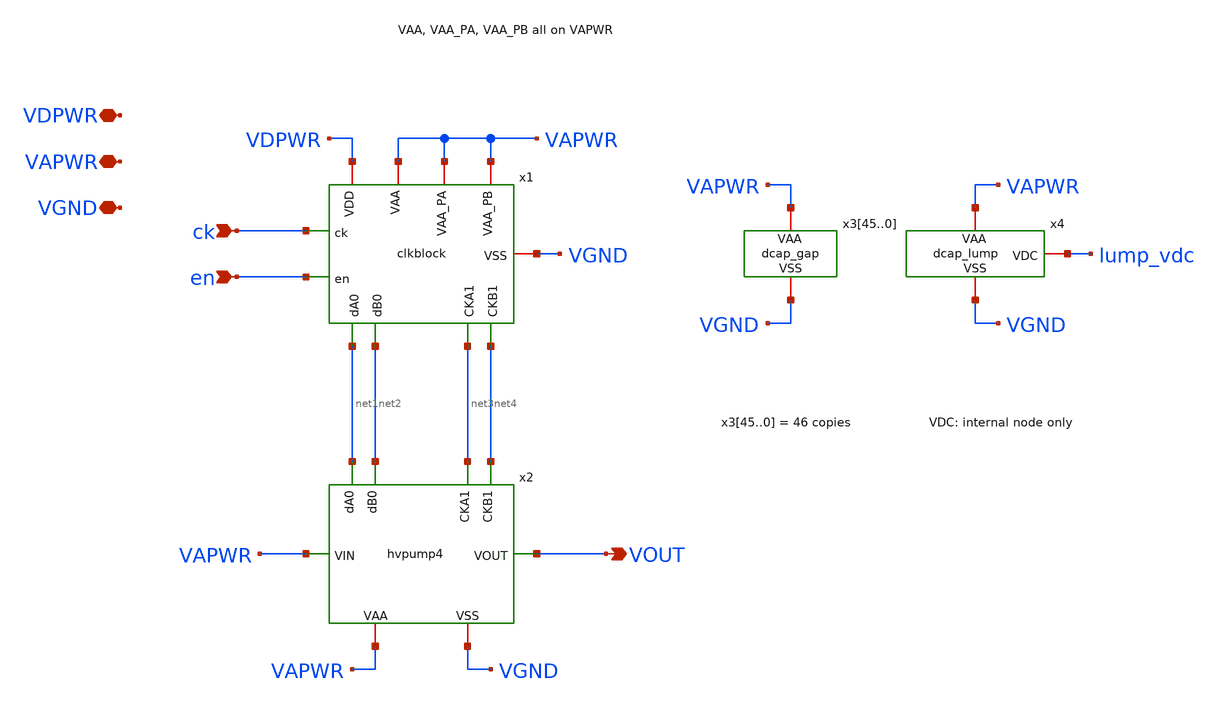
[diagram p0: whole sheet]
** sch_path: xschem/subsystem.sch
**.subckt subsystem VDPWR VAPWR VOUT en ck VGND
*.iopin VDPWR
*.iopin VAPWR
*.opin VOUT
*.ipin en
*.ipin ck
*.iopin VGND
x1 net3 net4 net1 net2 ck en VAPWR VDPWR VAPWR VAPWR VGND clkblock
x2 net1 net2 VAPWR VOUT net3 net4 VAPWR VGND hvpump4
x345 VGND VAPWR dcap_gap
x344 VGND VAPWR dcap_gap
x343 VGND VAPWR dcap_gap
x342 VGND VAPWR dcap_gap
x341 VGND VAPWR dcap_gap
x340 VGND VAPWR dcap_gap
x339 VGND VAPWR dcap_gap
x338 VGND VAPWR dcap_gap
x337 VGND VAPWR dcap_gap
x336 VGND VAPWR dcap_gap
x335 VGND VAPWR dcap_gap
x334 VGND VAPWR dcap_gap
x333 VGND VAPWR dcap_gap
x332 VGND VAPWR dcap_gap
x331 VGND VAPWR dcap_gap
x330 VGND VAPWR dcap_gap
x329 VGND VAPWR dcap_gap
x328 VGND VAPWR dcap_gap
x327 VGND VAPWR dcap_gap
x326 VGND VAPWR dcap_gap
x325 VGND VAPWR dcap_gap
x324 VGND VAPWR dcap_gap
x323 VGND VAPWR dcap_gap
x322 VGND VAPWR dcap_gap
x321 VGND VAPWR dcap_gap
x320 VGND VAPWR dcap_gap
x319 VGND VAPWR dcap_gap
x318 VGND VAPWR dcap_gap
x317 VGND VAPWR dcap_gap
x316 VGND VAPWR dcap_gap
x315 VGND VAPWR dcap_gap
x314 VGND VAPWR dcap_gap
x313 VGND VAPWR dcap_gap
x312 VGND VAPWR dcap_gap
x311 VGND VAPWR dcap_gap
x310 VGND VAPWR dcap_gap
x39 VGND VAPWR dcap_gap
x38 VGND VAPWR dcap_gap
x37 VGND VAPWR dcap_gap
x36 VGND VAPWR dcap_gap
x35 VGND VAPWR dcap_gap
x34 VGND VAPWR dcap_gap
x33 VGND VAPWR dcap_gap
x32 VGND VAPWR dcap_gap
x31 VGND VAPWR dcap_gap
x30 VGND VAPWR dcap_gap
x4 VGND VAPWR lump_vdc dcap_lump
**.ends
.end
